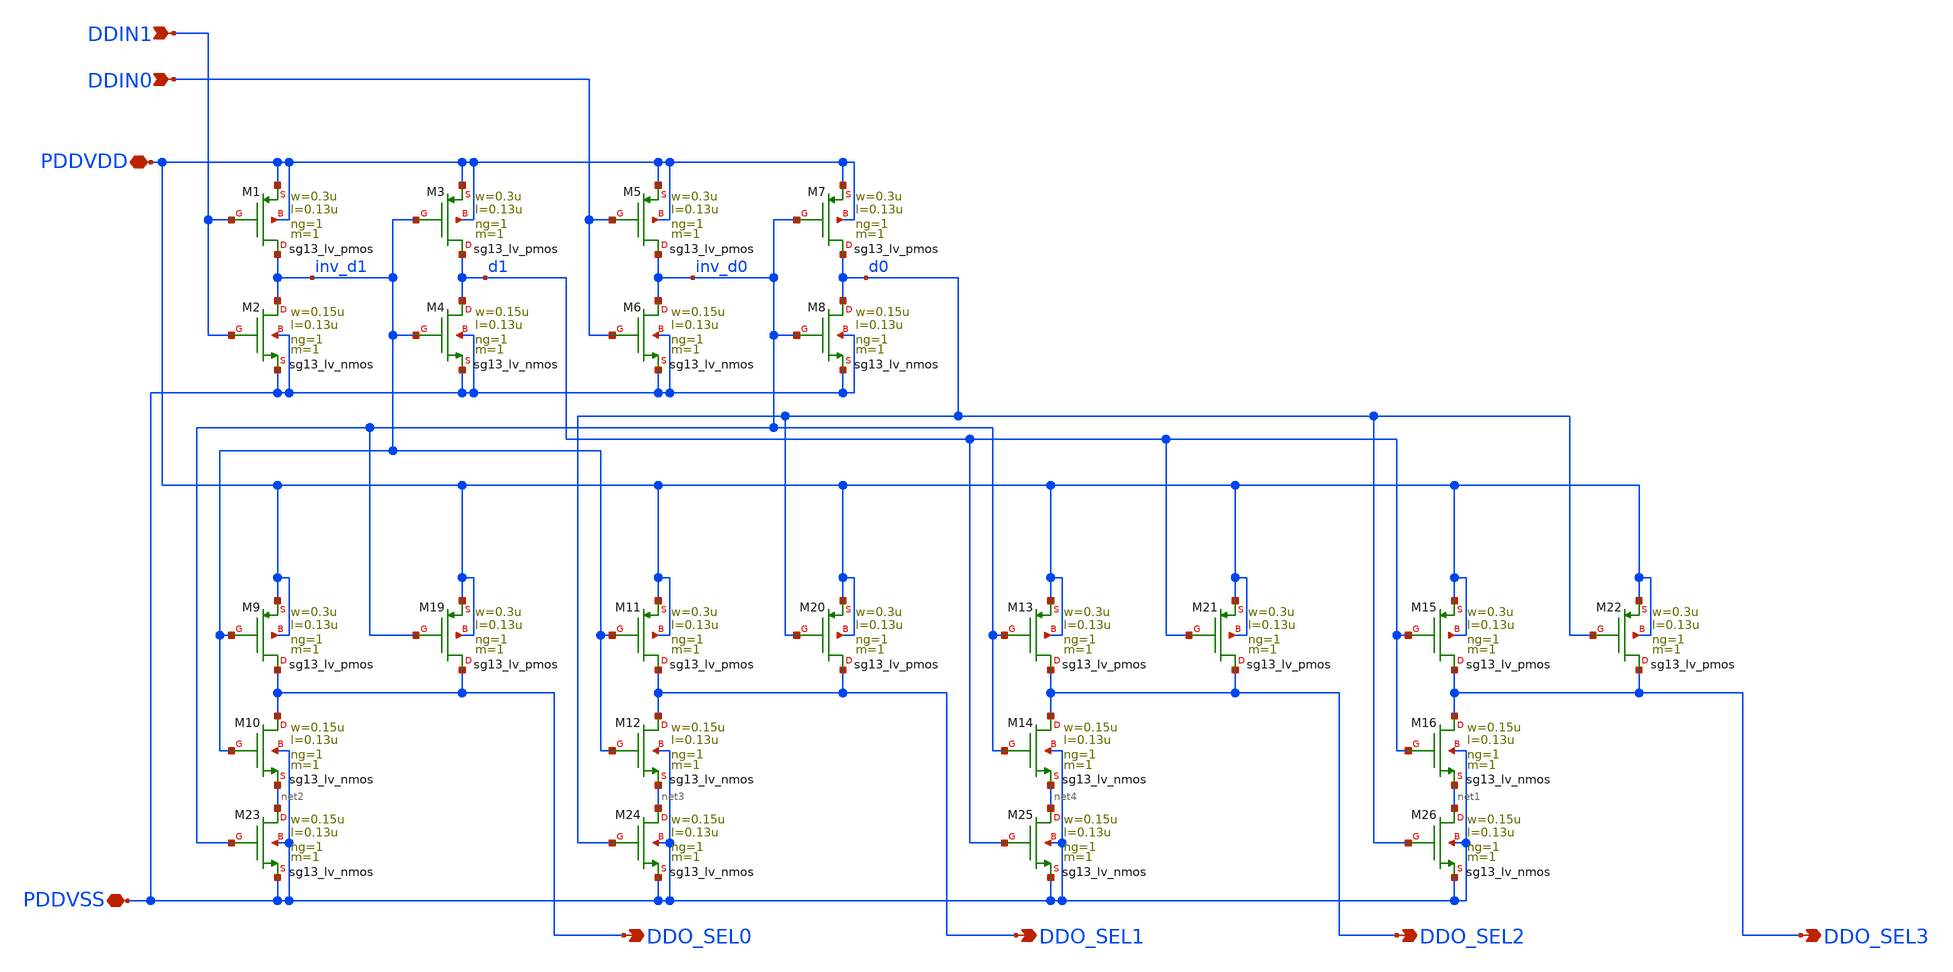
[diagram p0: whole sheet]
** sch_path: xschem/digital_decoder.sch
**.subckt digital_decoder DDIN1 DDIN0 DDO_SEL0 PDDVDD PDDVSS DDO_SEL1 DDO_SEL2 DDO_SEL3
*.ipin DDIN1
*.ipin DDIN0
*.opin DDO_SEL0
*.iopin PDDVDD
*.iopin PDDVSS
*.opin DDO_SEL1
*.opin DDO_SEL2
*.opin DDO_SEL3
XM1 inv_d1 DDIN1 PDDVDD PDDVDD sg13_lv_pmos w=0.3u l=0.13u ng=1 m=1 mm_ok=1
XM2 inv_d1 DDIN1 PDDVSS PDDVSS sg13_lv_nmos w=0.15u l=0.13u ng=1 m=1 mm_ok=1
XM3 d1 inv_d1 PDDVDD PDDVDD sg13_lv_pmos w=0.3u l=0.13u ng=1 m=1 mm_ok=1
XM4 d1 inv_d1 PDDVSS PDDVSS sg13_lv_nmos w=0.15u l=0.13u ng=1 m=1 mm_ok=1
XM5 inv_d0 DDIN0 PDDVDD PDDVDD sg13_lv_pmos w=0.3u l=0.13u ng=1 m=1 mm_ok=1
XM6 inv_d0 DDIN0 PDDVSS PDDVSS sg13_lv_nmos w=0.15u l=0.13u ng=1 m=1 mm_ok=1
XM7 d0 inv_d0 PDDVDD PDDVDD sg13_lv_pmos w=0.3u l=0.13u ng=1 m=1 mm_ok=1
XM8 d0 inv_d0 PDDVSS PDDVSS sg13_lv_nmos w=0.15u l=0.13u ng=1 m=1 mm_ok=1
XM9 DDO_SEL0 inv_d1 PDDVDD PDDVDD sg13_lv_pmos w=0.3u l=0.13u ng=1 m=1 mm_ok=1
XM10 DDO_SEL0 inv_d1 net2 PDDVSS sg13_lv_nmos w=0.15u l=0.13u ng=1 m=1 mm_ok=1
XM11 DDO_SEL1 inv_d1 PDDVDD PDDVDD sg13_lv_pmos w=0.3u l=0.13u ng=1 m=1 mm_ok=1
XM12 DDO_SEL1 inv_d1 net3 PDDVSS sg13_lv_nmos w=0.15u l=0.13u ng=1 m=1 mm_ok=1
XM13 DDO_SEL2 inv_d0 PDDVDD PDDVDD sg13_lv_pmos w=0.3u l=0.13u ng=1 m=1 mm_ok=1
XM14 DDO_SEL2 inv_d0 net4 PDDVSS sg13_lv_nmos w=0.15u l=0.13u ng=1 m=1 mm_ok=1
XM15 DDO_SEL3 d1 PDDVDD PDDVDD sg13_lv_pmos w=0.3u l=0.13u ng=1 m=1 mm_ok=1
XM16 DDO_SEL3 d1 net1 PDDVSS sg13_lv_nmos w=0.15u l=0.13u ng=1 m=1 mm_ok=1
XM19 DDO_SEL0 inv_d0 PDDVDD PDDVDD sg13_lv_pmos w=0.3u l=0.13u ng=1 m=1 mm_ok=1
XM20 DDO_SEL1 d0 PDDVDD PDDVDD sg13_lv_pmos w=0.3u l=0.13u ng=1 m=1 mm_ok=1
XM21 DDO_SEL2 d1 PDDVDD PDDVDD sg13_lv_pmos w=0.3u l=0.13u ng=1 m=1 mm_ok=1
XM22 DDO_SEL3 d0 PDDVDD PDDVDD sg13_lv_pmos w=0.3u l=0.13u ng=1 m=1 mm_ok=1
XM23 net2 inv_d0 PDDVSS PDDVSS sg13_lv_nmos w=0.15u l=0.13u ng=1 m=1 mm_ok=1
XM24 net3 d0 PDDVSS PDDVSS sg13_lv_nmos w=0.15u l=0.13u ng=1 m=1 mm_ok=1
XM25 net4 d1 PDDVSS PDDVSS sg13_lv_nmos w=0.15u l=0.13u ng=1 m=1 mm_ok=1
XM26 net1 d0 PDDVSS PDDVSS sg13_lv_nmos w=0.15u l=0.13u ng=1 m=1 mm_ok=1
**.ends
.end
